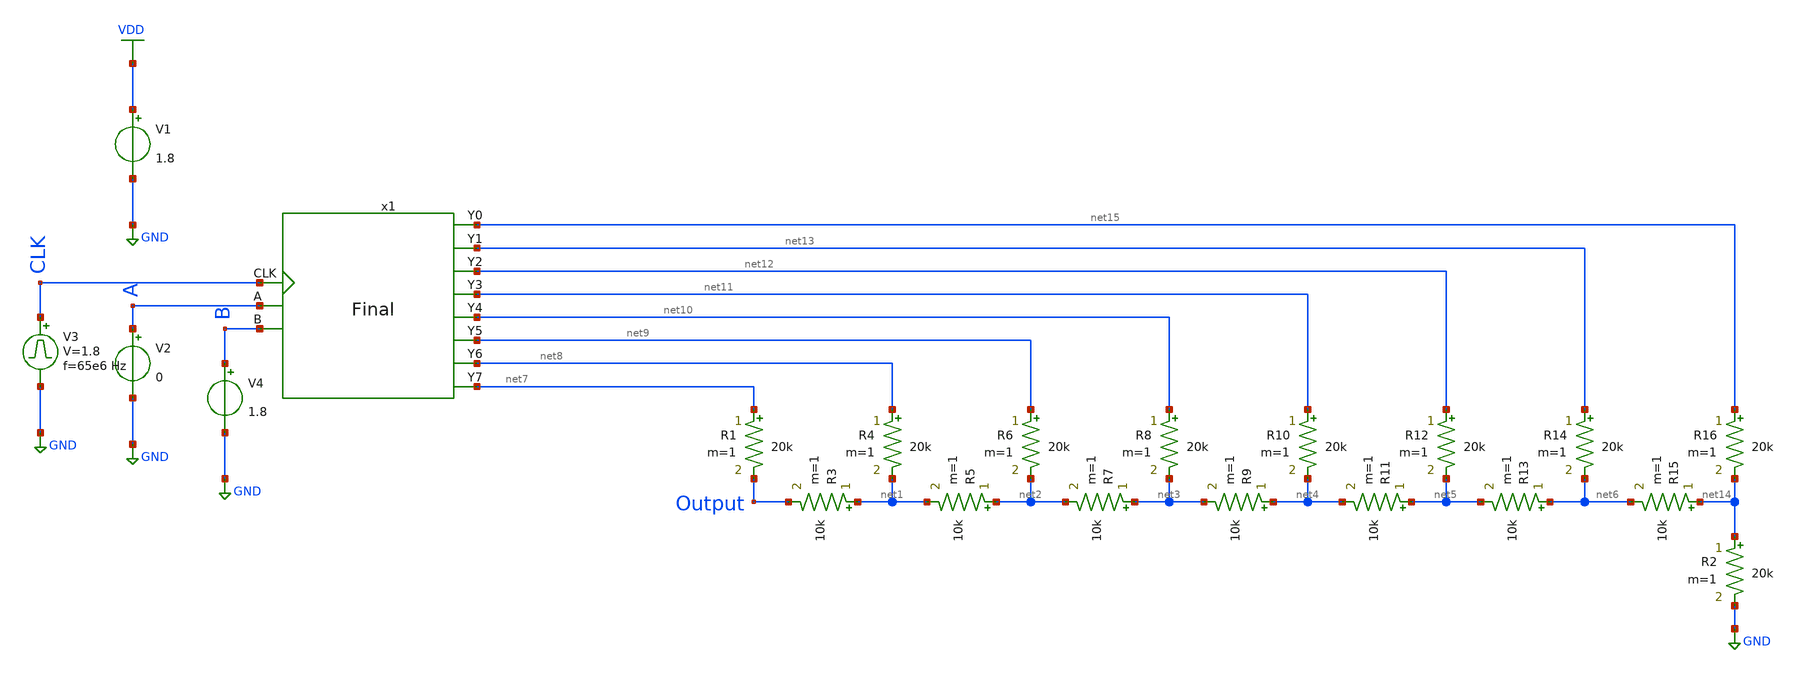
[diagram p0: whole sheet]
** sch_path: library/xschem/Final_tb.sch
**.subckt Final_tb
V1 VDD GND 1.8
V3 CLK GND pulse 0 1.8 '0.495/ 65e6 ' '0.01/65e6 ' '0.01/65e6 ' '0.49/65e6 ' '1/65e6 '
R2 net14 GND 20k m=1
R3 net1 Output 10k m=1
R5 net2 net1 10k m=1
R6 net9 net2 20k m=1
R7 net3 net2 10k m=1
R8 net10 net3 20k m=1
R9 net4 net3 10k m=1
R10 net11 net4 20k m=1
R11 net5 net4 10k m=1
R12 net12 net5 20k m=1
R13 net6 net5 10k m=1
R14 net13 net6 20k m=1
R1 net7 Output 20k m=1
R4 net8 net1 20k m=1
R15 net14 net6 10k m=1
R16 net15 net14 20k m=1
x1 CLK net15 net13 net12 net11 net10 net9 net8 net7 A B Final
V2 A GND 0
V4 B GND 1.8
**** begin user architecture code


.control
save all
tran 1n 500n
plot V(A) V(B)+2 V(Output)+4
.endc


** opencircuitdesign pdks install
.lib $::SKYWATER_MODELS/sky130.lib.spice tt


**** end user architecture code
**.ends

* expanding   symbol:  Final.sym # of pins=11
** sym_path: library/xschem/Final.sym
** sch_path: library/xschem/Final.sch
.subckt Final CLK Y0 Y1 Y2 Y3 Y4 Y5 Y6 Y7 A B
*.ipin CLK
*.ipin A
*.ipin B
*.opin Y0
*.opin Y1
*.opin Y2
*.opin Y3
*.opin Y4
*.opin Y5
*.opin Y6
*.opin Y7
x1 net1 net2 CLK net2 DFF
x2 net4 net3 net1 net3 DFF
x3 net6 net5 net4 net5 DFF
x4 net8 net7 net6 net7 DFF
x5 net10 net9 net8 net9 DFF
x6 net12 net11 net10 net11 DFF
x7 net14 net13 net12 net13 DFF
x8 net16 net15 net14 net15 DFF
x9 net18 net17 net16 net17 DFF
x15 net18 Y0 net26 net18 Y1 net25 net18 Y2 net24 net18 Y3 net23 net18 A Y4 net22 net18 Y5 net21
+ net18 Y6 net20 net18 Y7 net19 multiplexor
x10 net34 net26 net4 net33 net25 net6 net32 net24 net8 net31 net23 net10 net30 B net22 net12 net29
+ net21 net14 net28 net20 net16 net27 net19 net18 multiplexor
x11 net1 net34 net2 net4 net33 net3 net6 net32 net5 net8 net31 net7 net10 net17 net30 net9 net12
+ net29 net11 net14 net28 net13 net16 net27 net15 multiplexor
.ends


* expanding   symbol:  DFF.sym # of pins=4
** sym_path: library/xschem/DFF.sym
** sch_path: library/xschem/DFF.sch
.subckt DFF Q D CLK NOT_Q
*.ipin D
*.opin Q
*.opin NOT_Q
*.ipin CLK
x1 net2 net1 Q NOT_Q Dlatch
x2 D CLK net2 net3 Dlatch
x3 CLK net1 inv
.ends


* expanding   symbol:  multiplexor.sym # of pins=25
** sym_path: library/xschem/multiplexor.sym
** sch_path: library/xschem/multiplexor.sch
.subckt multiplexor A0 Y0 B0 A1 Y1 B1 A2 Y2 B2 A3 Y3 B3 A4 SEL Y4 B4 A5 Y5 B5 A6 Y6 B6 A7 Y7 B7
*.ipin A2
*.opin Y2
*.ipin B2
*.ipin A3
*.opin Y3
*.ipin B3
*.ipin A0
*.opin Y0
*.ipin B0
*.ipin A1
*.opin Y1
*.ipin B1
*.ipin A6
*.opin Y6
*.ipin B6
*.ipin A7
*.opin Y7
*.ipin B7
*.ipin A4
*.opin Y4
*.ipin B4
*.ipin A5
*.opin Y5
*.ipin B5
*.ipin SEL
x1 A2 net1 SEL nand2
x2 net17 net2 B2 nand2
x3 net1 Y2 net2 nand2
x4 A3 net3 SEL nand2
x5 net17 net4 B3 nand2
x6 net3 Y3 net4 nand2
x7 A0 net5 SEL nand2
x8 net17 net6 B0 nand2
x9 net5 Y0 net6 nand2
x10 A1 net7 SEL nand2
x11 net17 net8 B1 nand2
x12 net7 Y1 net8 nand2
x13 A6 net9 SEL nand2
x14 net17 net10 B6 nand2
x15 net9 Y6 net10 nand2
x16 A7 net11 SEL nand2
x17 net17 net12 B7 nand2
x18 net11 Y7 net12 nand2
x19 A4 net13 SEL nand2
x20 net17 net14 B4 nand2
x21 net13 Y4 net14 nand2
x22 A5 net15 SEL nand2
x23 net17 net16 B5 nand2
x24 net15 Y5 net16 nand2
x25 SEL net17 inv
.ends


* expanding   symbol:  Dlatch.sym # of pins=4
** sym_path: library/xschem/Dlatch.sym
** sch_path: library/xschem/Dlatch.sch
.subckt Dlatch D CLK Q NOT_Q
*.ipin D
*.ipin CLK
*.opin Q
*.opin NOT_Q
XM1 net1 CLK net2 GND sky130_fd_pr__nfet_01v8 L=0.15 W=1 nf=1 ad='int((nf+1)/2) * W/nf * 0.29' as='int((nf+2)/2) * W/nf * 0.29'
+ pd='2*int((nf+1)/2) * (W/nf + 0.29)' ps='2*int((nf+2)/2) * (W/nf + 0.29)' nrd='0.29 / W' nrs='0.29 / W'
+ sa=0 sb=0 sd=0 mult=1 m=1
XM2 net1 D VDD VDD sky130_fd_pr__pfet_01v8 L=0.15 W=1 nf=1 ad='int((nf+1)/2) * W/nf * 0.29' as='int((nf+2)/2) * W/nf * 0.29'
+ pd='2*int((nf+1)/2) * (W/nf + 0.29)' ps='2*int((nf+2)/2) * (W/nf + 0.29)' nrd='0.29 / W' nrs='0.29 / W'
+ sa=0 sb=0 sd=0 mult=1 m=1
XM3 net1 CLK VDD VDD sky130_fd_pr__pfet_01v8 L=0.15 W=1 nf=1 ad='int((nf+1)/2) * W/nf * 0.29' as='int((nf+2)/2) * W/nf * 0.29'
+ pd='2*int((nf+1)/2) * (W/nf + 0.29)' ps='2*int((nf+2)/2) * (W/nf + 0.29)' nrd='0.29 / W' nrs='0.29 / W'
+ sa=0 sb=0 sd=0 mult=1 m=1
XM4 net2 D GND GND sky130_fd_pr__nfet_01v8 L=0.15 W=1 nf=1 ad='int((nf+1)/2) * W/nf * 0.29' as='int((nf+2)/2) * W/nf * 0.29'
+ pd='2*int((nf+1)/2) * (W/nf + 0.29)' ps='2*int((nf+2)/2) * (W/nf + 0.29)' nrd='0.29 / W' nrs='0.29 / W'
+ sa=0 sb=0 sd=0 mult=1 m=1
XM5 Q NOT_Q net3 GND sky130_fd_pr__nfet_01v8 L=0.15 W=1 nf=1 ad='int((nf+1)/2) * W/nf * 0.29' as='int((nf+2)/2) * W/nf * 0.29'
+ pd='2*int((nf+1)/2) * (W/nf + 0.29)' ps='2*int((nf+2)/2) * (W/nf + 0.29)' nrd='0.29 / W' nrs='0.29 / W'
+ sa=0 sb=0 sd=0 mult=1 m=1
XM6 Q net1 VDD VDD sky130_fd_pr__pfet_01v8 L=0.15 W=1 nf=1 ad='int((nf+1)/2) * W/nf * 0.29' as='int((nf+2)/2) * W/nf * 0.29'
+ pd='2*int((nf+1)/2) * (W/nf + 0.29)' ps='2*int((nf+2)/2) * (W/nf + 0.29)' nrd='0.29 / W' nrs='0.29 / W'
+ sa=0 sb=0 sd=0 mult=1 m=1
XM7 Q NOT_Q VDD VDD sky130_fd_pr__pfet_01v8 L=0.15 W=1 nf=1 ad='int((nf+1)/2) * W/nf * 0.29' as='int((nf+2)/2) * W/nf * 0.29'
+ pd='2*int((nf+1)/2) * (W/nf + 0.29)' ps='2*int((nf+2)/2) * (W/nf + 0.29)' nrd='0.29 / W' nrs='0.29 / W'
+ sa=0 sb=0 sd=0 mult=1 m=1
XM8 net3 net1 GND GND sky130_fd_pr__nfet_01v8 L=0.15 W=1 nf=1 ad='int((nf+1)/2) * W/nf * 0.29' as='int((nf+2)/2) * W/nf * 0.29'
+ pd='2*int((nf+1)/2) * (W/nf + 0.29)' ps='2*int((nf+2)/2) * (W/nf + 0.29)' nrd='0.29 / W' nrs='0.29 / W'
+ sa=0 sb=0 sd=0 mult=1 m=1
XM9 NOT_Q net5 net4 GND sky130_fd_pr__nfet_01v8 L=0.15 W=1 nf=1 ad='int((nf+1)/2) * W/nf * 0.29' as='int((nf+2)/2) * W/nf * 0.29'
+ pd='2*int((nf+1)/2) * (W/nf + 0.29)' ps='2*int((nf+2)/2) * (W/nf + 0.29)' nrd='0.29 / W' nrs='0.29 / W'
+ sa=0 sb=0 sd=0 mult=1 m=1
XM10 NOT_Q Q VDD VDD sky130_fd_pr__pfet_01v8 L=0.15 W=1 nf=1 ad='int((nf+1)/2) * W/nf * 0.29' as='int((nf+2)/2) * W/nf * 0.29'
+ pd='2*int((nf+1)/2) * (W/nf + 0.29)' ps='2*int((nf+2)/2) * (W/nf + 0.29)' nrd='0.29 / W' nrs='0.29 / W'
+ sa=0 sb=0 sd=0 mult=1 m=1
XM11 NOT_Q net5 VDD VDD sky130_fd_pr__pfet_01v8 L=0.15 W=1 nf=1 ad='int((nf+1)/2) * W/nf * 0.29' as='int((nf+2)/2) * W/nf * 0.29'
+ pd='2*int((nf+1)/2) * (W/nf + 0.29)' ps='2*int((nf+2)/2) * (W/nf + 0.29)' nrd='0.29 / W' nrs='0.29 / W'
+ sa=0 sb=0 sd=0 mult=1 m=1
XM12 net4 Q GND GND sky130_fd_pr__nfet_01v8 L=0.15 W=1 nf=1 ad='int((nf+1)/2) * W/nf * 0.29' as='int((nf+2)/2) * W/nf * 0.29'
+ pd='2*int((nf+1)/2) * (W/nf + 0.29)' ps='2*int((nf+2)/2) * (W/nf + 0.29)' nrd='0.29 / W' nrs='0.29 / W'
+ sa=0 sb=0 sd=0 mult=1 m=1
XM13 net5 net7 net6 GND sky130_fd_pr__nfet_01v8 L=0.15 W=1 nf=1 ad='int((nf+1)/2) * W/nf * 0.29' as='int((nf+2)/2) * W/nf * 0.29'
+ pd='2*int((nf+1)/2) * (W/nf + 0.29)' ps='2*int((nf+2)/2) * (W/nf + 0.29)' nrd='0.29 / W' nrs='0.29 / W'
+ sa=0 sb=0 sd=0 mult=1 m=1
XM14 net5 CLK VDD VDD sky130_fd_pr__pfet_01v8 L=0.15 W=1 nf=1 ad='int((nf+1)/2) * W/nf * 0.29' as='int((nf+2)/2) * W/nf * 0.29'
+ pd='2*int((nf+1)/2) * (W/nf + 0.29)' ps='2*int((nf+2)/2) * (W/nf + 0.29)' nrd='0.29 / W' nrs='0.29 / W'
+ sa=0 sb=0 sd=0 mult=1 m=1
XM15 net5 net7 VDD VDD sky130_fd_pr__pfet_01v8 L=0.15 W=1 nf=1 ad='int((nf+1)/2) * W/nf * 0.29' as='int((nf+2)/2) * W/nf * 0.29'
+ pd='2*int((nf+1)/2) * (W/nf + 0.29)' ps='2*int((nf+2)/2) * (W/nf + 0.29)' nrd='0.29 / W' nrs='0.29 / W'
+ sa=0 sb=0 sd=0 mult=1 m=1
XM16 net6 CLK GND GND sky130_fd_pr__nfet_01v8 L=0.15 W=1 nf=1 ad='int((nf+1)/2) * W/nf * 0.29' as='int((nf+2)/2) * W/nf * 0.29'
+ pd='2*int((nf+1)/2) * (W/nf + 0.29)' ps='2*int((nf+2)/2) * (W/nf + 0.29)' nrd='0.29 / W' nrs='0.29 / W'
+ sa=0 sb=0 sd=0 mult=1 m=1
XM17 net7 D GND GND sky130_fd_pr__nfet_01v8 L=0.15 W=1 nf=1 ad='int((nf+1)/2) * W/nf * 0.29' as='int((nf+2)/2) * W/nf * 0.29'
+ pd='2*int((nf+1)/2) * (W/nf + 0.29)' ps='2*int((nf+2)/2) * (W/nf + 0.29)' nrd='0.29 / W' nrs='0.29 / W'
+ sa=0 sb=0 sd=0 mult=1 m=1
XM18 net7 D VDD VDD sky130_fd_pr__pfet_01v8 L=0.15 W=1 nf=1 ad='int((nf+1)/2) * W/nf * 0.29' as='int((nf+2)/2) * W/nf * 0.29'
+ pd='2*int((nf+1)/2) * (W/nf + 0.29)' ps='2*int((nf+2)/2) * (W/nf + 0.29)' nrd='0.29 / W' nrs='0.29 / W'
+ sa=0 sb=0 sd=0 mult=1 m=1
.ends


* expanding   symbol:  inv.sym # of pins=2
** sym_path: library/xschem/inv.sym
** sch_path: library/xschem/inv.sch
.subckt inv A Y
*.opin Y
*.ipin A
XM1 Y A GND GND sky130_fd_pr__nfet_01v8 L=0.15 W=1 nf=1 ad='int((nf+1)/2) * W/nf * 0.29' as='int((nf+2)/2) * W/nf * 0.29'
+ pd='2*int((nf+1)/2) * (W/nf + 0.29)' ps='2*int((nf+2)/2) * (W/nf + 0.29)' nrd='0.29 / W' nrs='0.29 / W'
+ sa=0 sb=0 sd=0 mult=1 m=1
XM2 Y A VDD VDD sky130_fd_pr__pfet_01v8 L=0.15 W=1 nf=1 ad='int((nf+1)/2) * W/nf * 0.29' as='int((nf+2)/2) * W/nf * 0.29'
+ pd='2*int((nf+1)/2) * (W/nf + 0.29)' ps='2*int((nf+2)/2) * (W/nf + 0.29)' nrd='0.29 / W' nrs='0.29 / W'
+ sa=0 sb=0 sd=0 mult=1 m=1
.ends


* expanding   symbol:  nand2.sym # of pins=3
** sym_path: library/xschem/nand2.sym
** sch_path: library/xschem/nand2.sch
.subckt nand2 A Y B
*.opin Y
*.ipin A
*.ipin B
XM1 Y B net1 GND sky130_fd_pr__nfet_01v8 L=0.15 W=1 nf=1 ad='int((nf+1)/2) * W/nf * 0.29' as='int((nf+2)/2) * W/nf * 0.29'
+ pd='2*int((nf+1)/2) * (W/nf + 0.29)' ps='2*int((nf+2)/2) * (W/nf + 0.29)' nrd='0.29 / W' nrs='0.29 / W'
+ sa=0 sb=0 sd=0 mult=1 m=1
XM2 Y B VDD VDD sky130_fd_pr__pfet_01v8 L=0.15 W=1 nf=1 ad='int((nf+1)/2) * W/nf * 0.29' as='int((nf+2)/2) * W/nf * 0.29'
+ pd='2*int((nf+1)/2) * (W/nf + 0.29)' ps='2*int((nf+2)/2) * (W/nf + 0.29)' nrd='0.29 / W' nrs='0.29 / W'
+ sa=0 sb=0 sd=0 mult=1 m=1
XM3 Y A VDD VDD sky130_fd_pr__pfet_01v8 L=0.15 W=1 nf=1 ad='int((nf+1)/2) * W/nf * 0.29' as='int((nf+2)/2) * W/nf * 0.29'
+ pd='2*int((nf+1)/2) * (W/nf + 0.29)' ps='2*int((nf+2)/2) * (W/nf + 0.29)' nrd='0.29 / W' nrs='0.29 / W'
+ sa=0 sb=0 sd=0 mult=1 m=1
XM4 net1 A GND GND sky130_fd_pr__nfet_01v8 L=0.15 W=1 nf=1 ad='int((nf+1)/2) * W/nf * 0.29' as='int((nf+2)/2) * W/nf * 0.29'
+ pd='2*int((nf+1)/2) * (W/nf + 0.29)' ps='2*int((nf+2)/2) * (W/nf + 0.29)' nrd='0.29 / W' nrs='0.29 / W'
+ sa=0 sb=0 sd=0 mult=1 m=1
.ends

.GLOBAL VDD
.GLOBAL GND
.end
